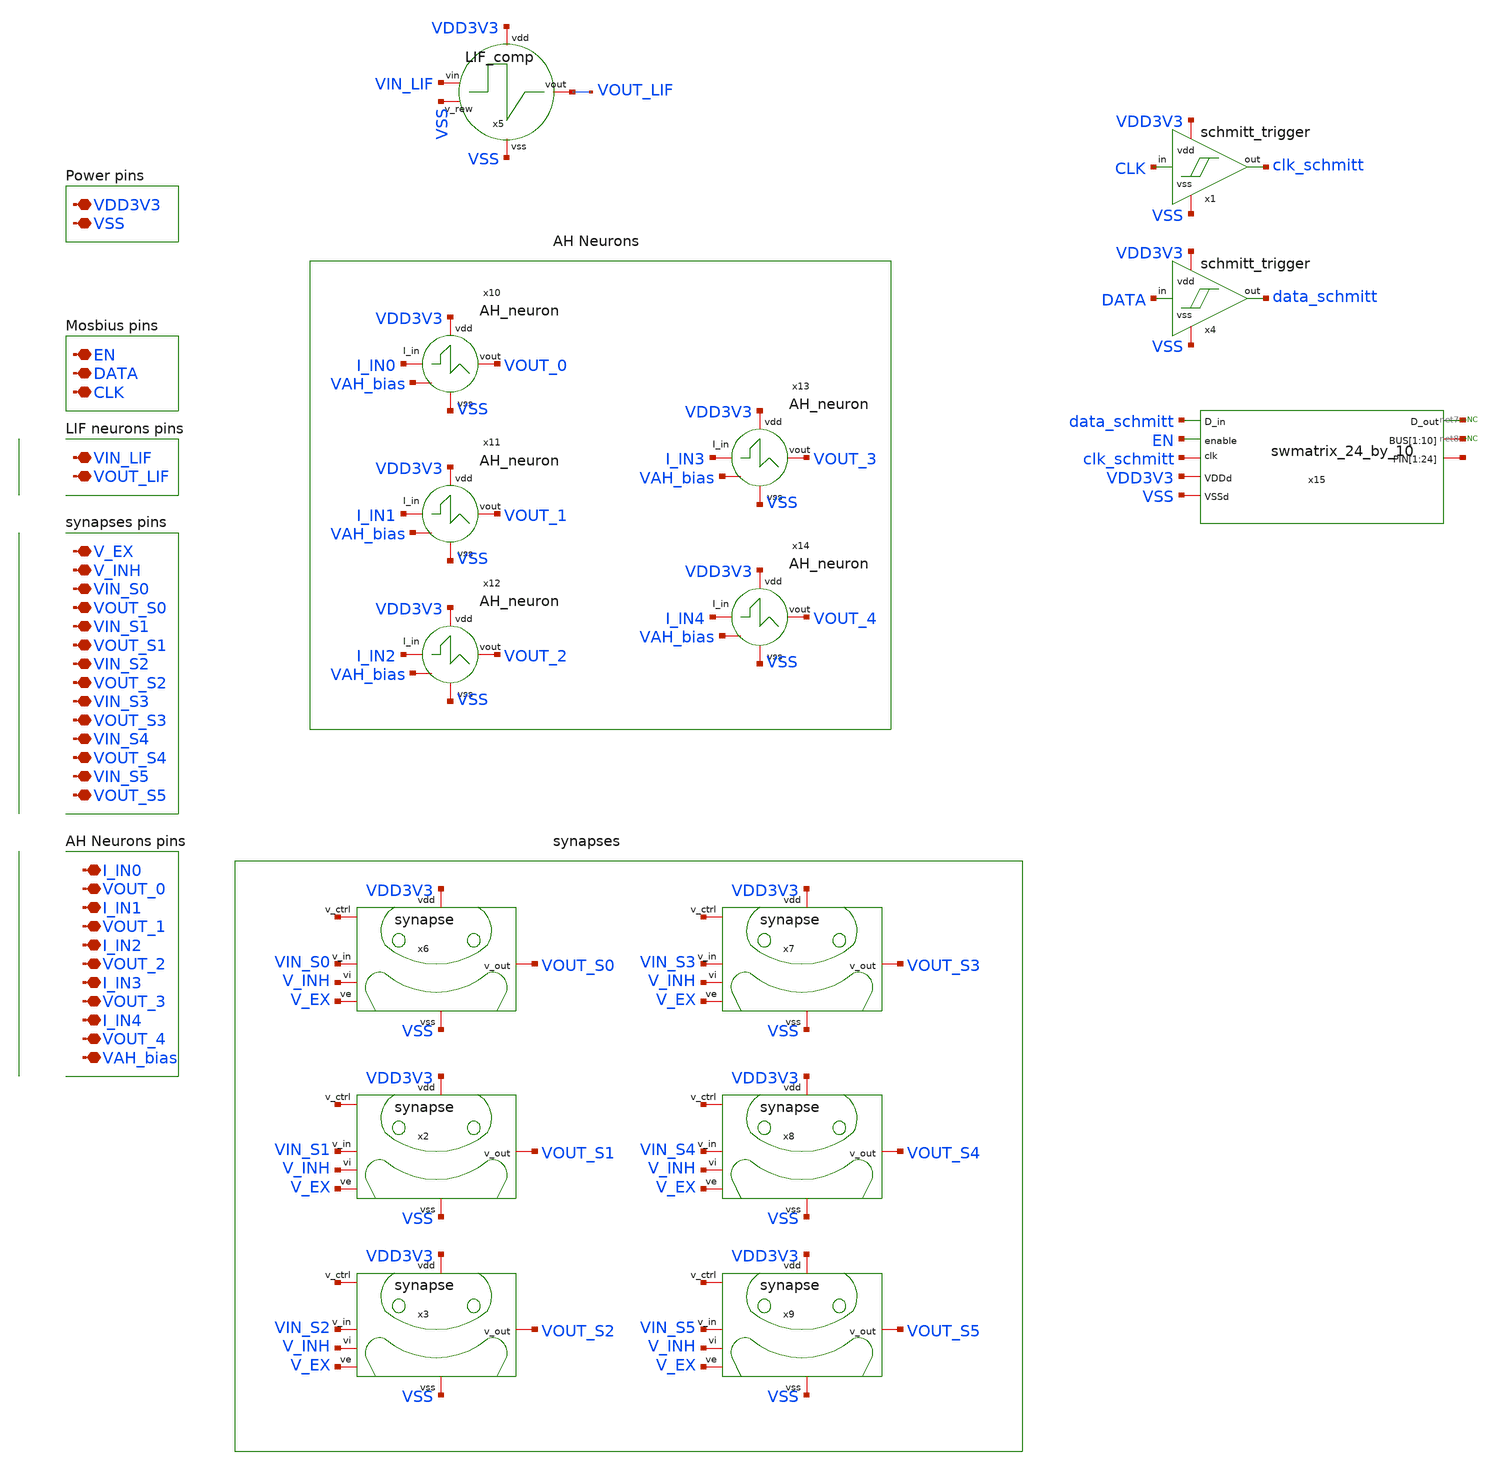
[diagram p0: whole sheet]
** sch_path: designs/klayout/layout_top/top.sch
**.subckt top I_IN0 VOUT_0 I_IN1 VOUT_1 I_IN2 VOUT_2 I_IN3 VOUT_3 VDD3V3 VSS VIN_LIF VOUT_LIF V_EX
*+ V_INH VIN_S0 VOUT_S0 VIN_S1 VOUT_S1 VIN_S2 VOUT_S2 EN DATA CLK I_IN4 VOUT_4 VIN_S3 VOUT_S3 VIN_S4 VOUT_S4
*+ VIN_S5 VOUT_S5 VAH_bias
*.iopin I_IN0
*.iopin VOUT_0
*.iopin I_IN1
*.iopin VOUT_1
*.iopin I_IN2
*.iopin VOUT_2
*.iopin I_IN3
*.iopin VOUT_3
*.iopin VDD3V3
*.iopin VSS
*.iopin VIN_LIF
*.iopin VOUT_LIF
*.iopin V_EX
*.iopin V_INH
*.iopin VIN_S0
*.iopin VOUT_S0
*.iopin VIN_S1
*.iopin VOUT_S1
*.iopin VIN_S2
*.iopin VOUT_S2
*.iopin EN
*.iopin DATA
*.iopin CLK
*.iopin I_IN4
*.iopin VOUT_4
*.iopin VIN_S3
*.iopin VOUT_S3
*.iopin VIN_S4
*.iopin VOUT_S4
*.iopin VIN_S5
*.iopin VOUT_S5
*.iopin VAH_bias
x5 VDD3V3 VSS VIN_LIF VSS VOUT_LIF LIF_comp
x6 VDD3V3 VIN_S0 V_EX net1 VOUT_S0 V_INH VSS synapse
x2 VDD3V3 VIN_S1 V_EX net2 VOUT_S1 V_INH VSS synapse
x3 VDD3V3 VIN_S2 V_EX net3 VOUT_S2 V_INH VSS synapse
x7 VDD3V3 VIN_S3 V_EX net4 VOUT_S3 V_INH VSS synapse
x8 VDD3V3 VIN_S4 V_EX net5 VOUT_S4 V_INH VSS synapse
x9 VDD3V3 VIN_S5 V_EX net6 VOUT_S5 V_INH VSS synapse
x10 VDD3V3 I_IN0 VOUT_0 VSS VAH_bias AH_neuron
x11 VDD3V3 I_IN1 VOUT_1 VSS VAH_bias AH_neuron
x12 VDD3V3 I_IN2 VOUT_2 VSS VAH_bias AH_neuron
x13 VDD3V3 I_IN3 VOUT_3 VSS VAH_bias AH_neuron
x14 VDD3V3 I_IN4 VOUT_4 VSS VAH_bias AH_neuron
x1 clk_schmitt CLK VDD3V3 VSS schmitt_trigger
x4 data_schmitt DATA VDD3V3 VSS schmitt_trigger
x15 net7 net8 net8 net8 net8 net8 net8 net8 net8 net8 net8 net9[23] net9[22] net9[21] net9[20]
+ net9[19] net9[18] net9[17] net9[16] net9[15] net9[14] net9[13] net9[12] net9[11] net9[10] net9[9] net9[8]
+ net9[7] net9[6] net9[5] net9[4] net9[3] net9[2] net9[1] net9[0] data_schmitt VDD3V3 EN VSS clk_schmitt
+ swmatrix_24_by_10
* noconn #net7
* noconn #net8
**.ends
.end
